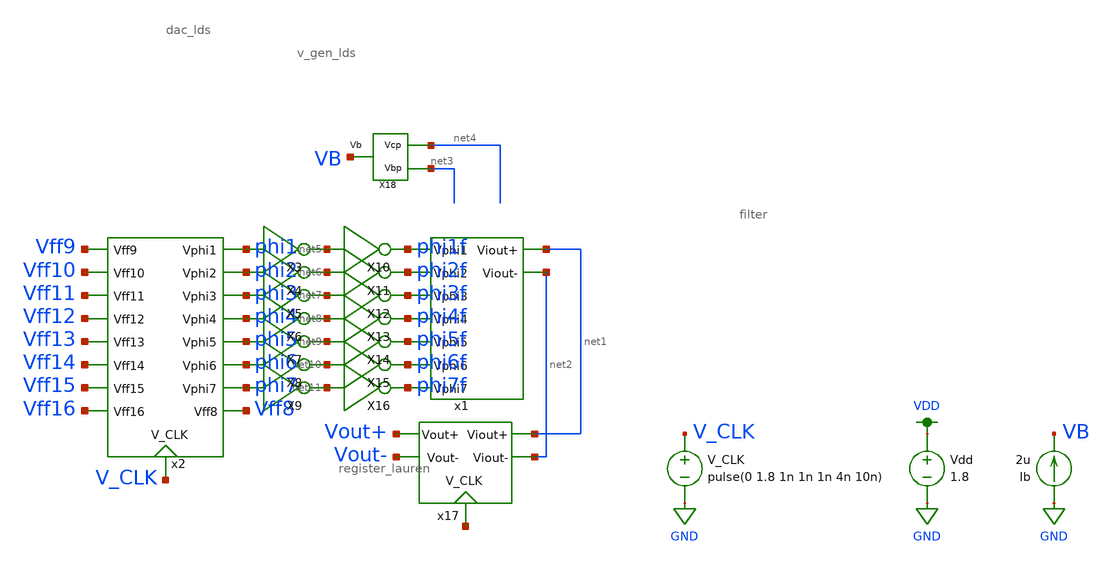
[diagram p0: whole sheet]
** sch_path: simulation/archived/combined_simulations/register_dac_mc_andrew_lds.sch
**.subckt register_dac_mc_andrew_lds
V_CLK V_CLK GND pulse(0 1.8 1n 1n 1n 4n 10n)
Vdd VDD GND 1.8
x1 phi1f phi2f phi3f phi4f phi5f phi6f phi7f net1 net2 dac_lds
x2 Vff10 Vff11 Vff12 Vff13 Vff14 Vff16 Vff15 Vff9 phi1 phi2 phi3 phi4 phi5 phi6 phi7 Vff8 V_CLK
+ register_lauren
X3 phi1 net5 inverter
X4 phi2 net6 inverter
X5 phi3 net7 inverter
X6 phi4 net8 inverter
X7 phi5 net9 inverter
X8 phi6 net10 inverter
X9 phi7 net11 inverter
X10 net5 phi1f inverter
X11 net6 phi2f inverter
X12 net7 phi3f inverter
X13 net8 phi4f inverter
X14 net9 phi5f inverter
X15 net10 phi6f inverter
X16 net11 phi7f inverter
x17 net1 net2 Vout+ Vout- net12 filter
X18 net4 net3 VB v_gen_lds
Ib GND VB 2u
**** begin user architecture code

.option wnflag=1
.param MC_SWITCH=1.0
.lib ~/skywater/skywater-pdk/libraries/sky130_fd_pr_ngspice/latest/models/sky130.lib.spice tt



.ic v(phi1)=0 v(phi2)=0 v(phi3)=0 v(phi4)=0 v(phi5)=0 v(phi6)=0 v(phi7)=0 v(Vff8)=0 v(Vff9)=1.8
+ v(Vff10)=1.8 v(Vff11)=1.8 v(Vff12)=1.8 v(Vff13)=1.8 v(Vff14)=1.8 v(Vff15)=1.8 v(Vff16)=1.8
.control
  set wr_vecnames
  set wr_singlescale

  let mc_runs = 10
  let run = 1
  dowhile run <= mc_runs
    tran 0.1n 1u
    wrdata ~/Documents/VLSI_Sine_Gen/simulation/sim_data/register_dac_mc_lds_bias_{$&run}.txt v(Vout+)
+ v(Vout-) v(Vout+)-v(Vout-)
    reset
    let run = run + 1
  end
  quit
.endc


**** end user architecture code
**.ends
.GLOBAL GND
.GLOBAL VDD
.end
